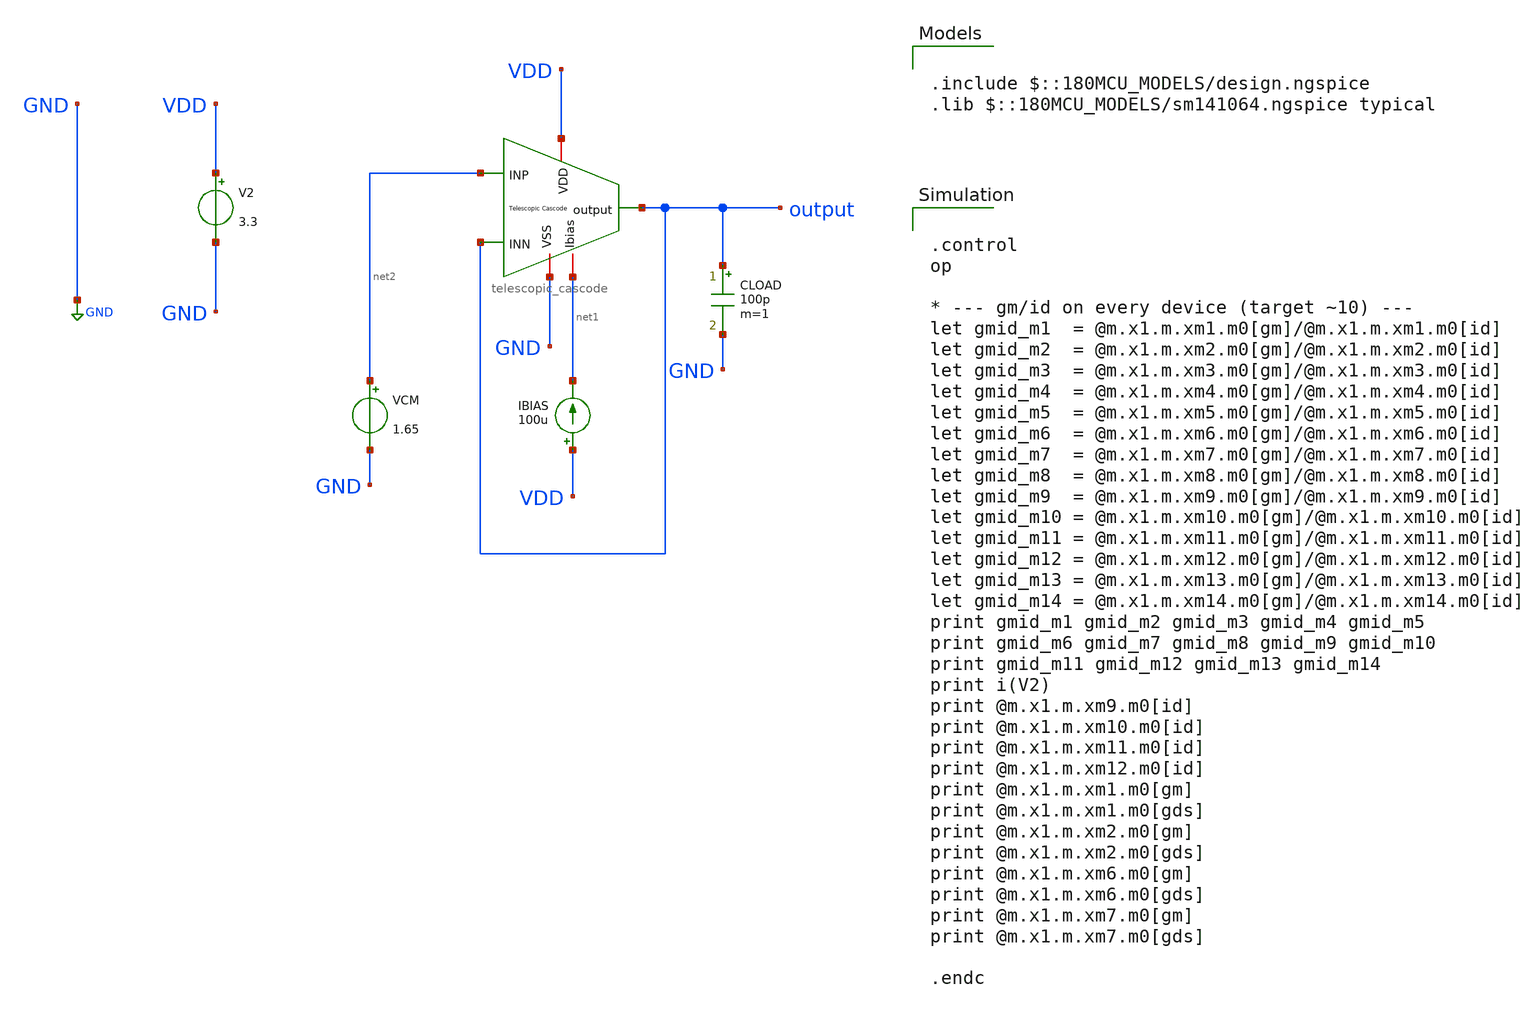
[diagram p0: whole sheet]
** sch_path: designs/libs/core_amps/ota_telescopic/tb/telescopic_op_gmid_tb.sch
**.subckt telescopic_op_gmid_tb
IBIAS VDD net1 100u
V2 VDD GND 3.3
CLOAD output GND 100p m=1
VCM net2 GND 1.65
x1 VDD output output net2 GND net1 telescopic_cascode
**** begin user architecture code

.include $::180MCU_MODELS/design.ngspice
.lib $::180MCU_MODELS/sm141064.ngspice typical



.control
op

* --- gm/id on every device (target ~10) ---
let gmid_m1  = @m.x1.m.xm1.m0[gm]/@m.x1.m.xm1.m0[id]
let gmid_m2  = @m.x1.m.xm2.m0[gm]/@m.x1.m.xm2.m0[id]
let gmid_m3  = @m.x1.m.xm3.m0[gm]/@m.x1.m.xm3.m0[id]
let gmid_m4  = @m.x1.m.xm4.m0[gm]/@m.x1.m.xm4.m0[id]
let gmid_m5  = @m.x1.m.xm5.m0[gm]/@m.x1.m.xm5.m0[id]
let gmid_m6  = @m.x1.m.xm6.m0[gm]/@m.x1.m.xm6.m0[id]
let gmid_m7  = @m.x1.m.xm7.m0[gm]/@m.x1.m.xm7.m0[id]
let gmid_m8  = @m.x1.m.xm8.m0[gm]/@m.x1.m.xm8.m0[id]
let gmid_m9  = @m.x1.m.xm9.m0[gm]/@m.x1.m.xm9.m0[id]
let gmid_m10 = @m.x1.m.xm10.m0[gm]/@m.x1.m.xm10.m0[id]
let gmid_m11 = @m.x1.m.xm11.m0[gm]/@m.x1.m.xm11.m0[id]
let gmid_m12 = @m.x1.m.xm12.m0[gm]/@m.x1.m.xm12.m0[id]
let gmid_m13 = @m.x1.m.xm13.m0[gm]/@m.x1.m.xm13.m0[id]
let gmid_m14 = @m.x1.m.xm14.m0[gm]/@m.x1.m.xm14.m0[id]
print gmid_m1 gmid_m2 gmid_m3 gmid_m4 gmid_m5
print gmid_m6 gmid_m7 gmid_m8 gmid_m9 gmid_m10
print gmid_m11 gmid_m12 gmid_m13 gmid_m14
print i(V2)
print @m.x1.m.xm9.m0[id]
print @m.x1.m.xm10.m0[id]
print @m.x1.m.xm11.m0[id]
print @m.x1.m.xm12.m0[id]
print @m.x1.m.xm1.m0[gm]
print @m.x1.m.xm1.m0[gds]
print @m.x1.m.xm2.m0[gm]
print @m.x1.m.xm2.m0[gds]
print @m.x1.m.xm6.m0[gm]
print @m.x1.m.xm6.m0[gds]
print @m.x1.m.xm7.m0[gm]
print @m.x1.m.xm7.m0[gds]

.endc


**** end user architecture code
**.ends
.GLOBAL GND
.end
